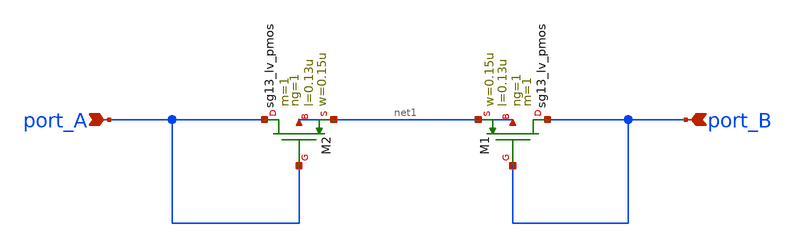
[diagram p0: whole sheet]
** sch_path: analog-db/templates/pseudo_resistor/pseudo-resistor-c-well-only.sch
* Copyright 2026 MacAnalog Research Group
**.subckt pseudo-resistor-c-well-only port_A port_B
*.ipin port_A
*.ipin port_B
XM1 port_B port_B net1 net1 sg13_lv_pmos w=0.15u l=0.13u ng=1 m=1 mm_ok=1
XM2 port_A port_A net1 net1 sg13_lv_pmos w=0.15u l=0.13u ng=1 m=1 mm_ok=1
**.ends
.end
